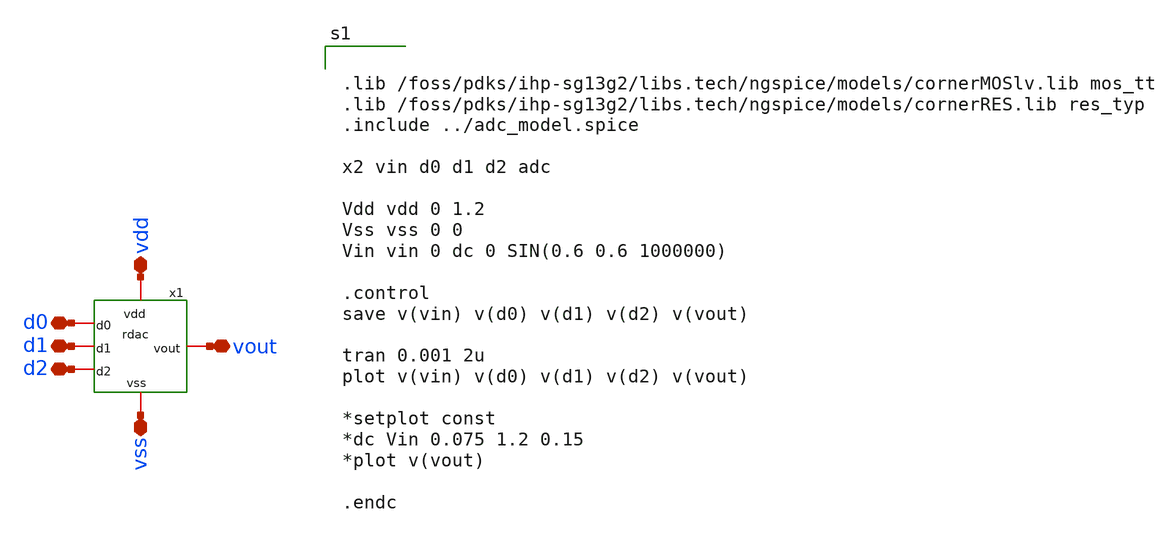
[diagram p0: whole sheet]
** sch_path: xschem/rdac_tb.sch
**.subckt rdac_tb vout vss d0 d1 d2 vdd
*.iopin vout
*.iopin vss
*.iopin d0
*.iopin d1
*.iopin d2
*.iopin vdd
x1 vdd d0 vout d1 d2 vss rdac
**** begin user architecture code


.lib /foss/pdks/ihp-sg13g2/libs.tech/ngspice/models/cornerMOSlv.lib mos_tt
.lib /foss/pdks/ihp-sg13g2/libs.tech/ngspice/models/cornerRES.lib res_typ
.include ../adc_model.spice

x2 vin d0 d1 d2 adc

Vdd vdd 0 1.2
Vss vss 0 0
Vin vin 0 dc 0 SIN(0.6 0.6 1000000)

.control
save v(vin) v(d0) v(d1) v(d2) v(vout)

tran 0.001 2u
plot v(vin) v(d0) v(d1) v(d2) v(vout)

*setplot const
*dc Vin 0.075 1.2 0.15
*plot v(vout)

.endc


**** end user architecture code
**.ends

* expanding   symbol:  rdac.sym # of pins=6
** sym_path: xschem/rdac.sym
** sch_path: xschem/rdac.sch
.subckt rdac vdd d0 vout d1 d2 vss
*.iopin vout
*.iopin vdd
*.iopin d0
*.iopin vss
*.iopin d1
*.iopin d2
x1 vdd d0 net5 vss inverter
x2 vdd d1 net4 vss inverter
x3 vdd d2 net1 vss inverter
XR1 net1 vout sub! rhigh w=0.5e-6 l=10.0e-6 m=1 b=0 mm_ok=1
XR2 net4 net2 sub! rhigh w=0.5e-6 l=10.0e-6 m=1 b=0 mm_ok=1
XR3 net5 net3 sub! rhigh w=0.5e-6 l=10.0e-6 m=1 b=0 mm_ok=1
XR4 vss net3 sub! rhigh w=0.5e-6 l=10.0e-6 m=1 b=0 mm_ok=1
XR5 vout net2 sub! rhigh w=0.5e-6 l=5.0e-6 m=1 b=0 mm_ok=1
XR6 net2 net3 sub! rhigh w=0.5e-6 l=5.0e-6 m=1 b=0 mm_ok=1
.ends


* expanding   symbol:  inverter.sym # of pins=4
** sym_path: xschem/inverter.sym
** sch_path: xschem/inverter.sch
.subckt inverter vdd vin vout vss
*.iopin vout
*.iopin vss
*.iopin vin
*.iopin vdd
XM1 vout vin vss vss sg13_lv_nmos w=1.5u l=0.13u ng=1 m=1 mm_ok=1
XM2 vout vin vdd vdd sg13_lv_pmos w=3.0u l=0.13u ng=1 m=1 mm_ok=1
.ends

.end
